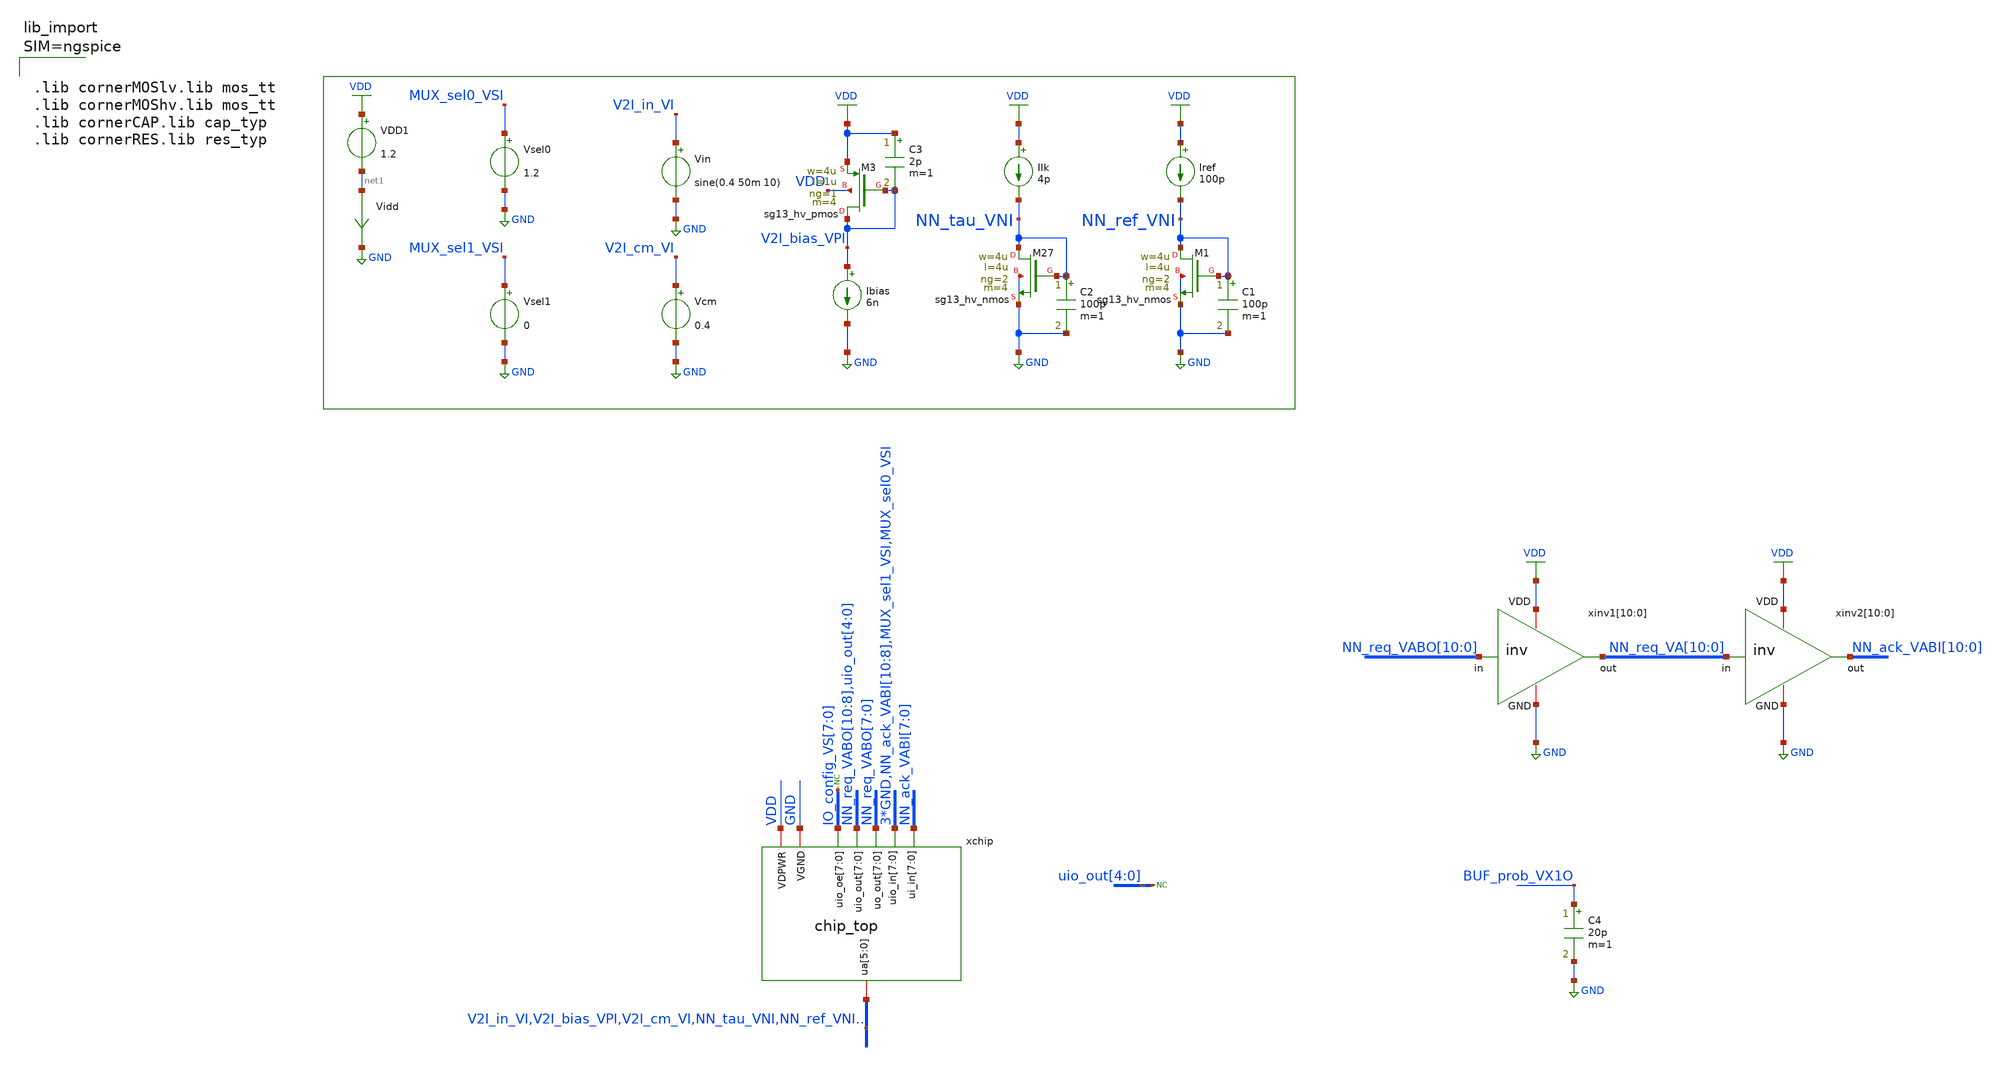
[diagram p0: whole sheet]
** sch_path: xschem/ncs-dpi-adexp/xschem/chip_top_tb.sch
**.subckt chip_top_tb
Ilk VDD NN_tau_VNI 4p
VDD1 VDD net1 1.2
Iref VDD NN_ref_VNI 100p
Vidd net1 GND 0
.save i(vidd)
XM27 NN_tau_VNI NN_tau_VNI GND GND sg13_hv_nmos w=4u l=4u ng=2 m=4 mm_ok=1
C2 NN_tau_VNI GND 100p m=1
XM1 NN_ref_VNI NN_ref_VNI GND GND sg13_hv_nmos w=4u l=4u ng=2 m=4 mm_ok=1
C1 NN_ref_VNI GND 100p m=1
XM3 V2I_bias_VPI V2I_bias_VPI VDD VDD sg13_hv_pmos w=4u l=1u ng=1 m=4 mm_ok=1
C3 VDD V2I_bias_VPI 2p m=1
Ibias V2I_bias_VPI GND 6n
Vcm V2I_cm_VI GND 0.4
Vin V2I_in_VI GND sine(0.4 50m 10)
C4 BUF_prob_VX1O GND 20p m=1
xinv1[10] VDD NN_req_VA[10] NN_req_VABO[10] GND inv
xinv1[9] VDD NN_req_VA[9] NN_req_VABO[9] GND inv
xinv1[8] VDD NN_req_VA[8] NN_req_VABO[8] GND inv
xinv1[7] VDD NN_req_VA[7] NN_req_VABO[7] GND inv
xinv1[6] VDD NN_req_VA[6] NN_req_VABO[6] GND inv
xinv1[5] VDD NN_req_VA[5] NN_req_VABO[5] GND inv
xinv1[4] VDD NN_req_VA[4] NN_req_VABO[4] GND inv
xinv1[3] VDD NN_req_VA[3] NN_req_VABO[3] GND inv
xinv1[2] VDD NN_req_VA[2] NN_req_VABO[2] GND inv
xinv1[1] VDD NN_req_VA[1] NN_req_VABO[1] GND inv
xinv1[0] VDD NN_req_VA[0] NN_req_VABO[0] GND inv
xinv2[10] VDD NN_ack_VABI[10] NN_req_VA[10] GND inv
xinv2[9] VDD NN_ack_VABI[9] NN_req_VA[9] GND inv
xinv2[8] VDD NN_ack_VABI[8] NN_req_VA[8] GND inv
xinv2[7] VDD NN_ack_VABI[7] NN_req_VA[7] GND inv
xinv2[6] VDD NN_ack_VABI[6] NN_req_VA[6] GND inv
xinv2[5] VDD NN_ack_VABI[5] NN_req_VA[5] GND inv
xinv2[4] VDD NN_ack_VABI[4] NN_req_VA[4] GND inv
xinv2[3] VDD NN_ack_VABI[3] NN_req_VA[3] GND inv
xinv2[2] VDD NN_ack_VABI[2] NN_req_VA[2] GND inv
xinv2[1] VDD NN_ack_VABI[1] NN_req_VA[1] GND inv
xinv2[0] VDD NN_ack_VABI[0] NN_req_VA[0] GND inv
xchip NN_ack_VABI[7] NN_ack_VABI[6] NN_ack_VABI[5] NN_ack_VABI[4] NN_ack_VABI[3] NN_ack_VABI[2]
+ NN_ack_VABI[1] NN_ack_VABI[0] V2I_in_VI V2I_bias_VPI V2I_cm_VI NN_tau_VNI NN_ref_VNI BUF_prob_VX1O VDD
+ NN_req_VABO[7] NN_req_VABO[6] NN_req_VABO[5] NN_req_VABO[4] NN_req_VABO[3] NN_req_VABO[2] NN_req_VABO[1]
+ NN_req_VABO[0] GND GND GND GND NN_ack_VABI[10] NN_ack_VABI[9] NN_ack_VABI[8] MUX_sel1_VSI MUX_sel0_VSI
+ NN_req_VABO[10] NN_req_VABO[9] NN_req_VABO[8] uio_out[4] uio_out[3] uio_out[2] uio_out[1] uio_out[0]
+ IO_config_VS[7] IO_config_VS[6] IO_config_VS[5] IO_config_VS[4] IO_config_VS[3] IO_config_VS[2] IO_config_VS[1]
+ IO_config_VS[0] chip_top
* noconn IO_config_VS[7:0]
* noconn uio_out[4:0]
Vsel1 MUX_sel1_VSI GND 0
Vsel0 MUX_sel0_VSI GND 1.2
**** begin user architecture code



.param temp=27

.ic V(NN_req_VABO[10])=1.2 V(NN_req_VABO[9])=1.2 V(NN_req_VABO[8])=1.2 V(NN_req_VABO[7])=1.2
+ V(NN_req_VABO[6])=1.2 V(NN_req_VABO[5])=1.2 V(NN_req_VABO[4])=1.2 V(NN_req_VABO[3])=1.2 V(NN_req_VABO[2])=1.2
+ V(NN_req_VABO[1])=1.2 V(NN_req_VABO[0])=1.2
.ic V(NN_ack_VABI[10])=1.2 V(NN_ack_VABI[9])=1.2 V(NN_ack_VABI[8])=1.2 V(NN_ack_VABI[7])=1.2
+ V(NN_ack_VABI[6])=1.2 V(NN_ack_VABI[5])=1.2 V(NN_ack_VABI[4])=1.2 V(NN_ack_VABI[3])=1.2 V(NN_ack_VABI[2])=1.2
+ V(NN_ack_VABI[1])=1.2 V(NN_ack_VABI[0])=1.2
.ic V(xchip.NN_mem_VNT[10])=0 V(xchip.NN_mem_VNT[9])=0 V(xchip.NN_mem_VNT[8])=0
+ V(xchip.NN_mem_VNT[7])=0 V(xchip.NN_mem_VNT[6])=0 V(xchip.NN_mem_VNT[5])=0 V(xchip.NN_mem_VNT[4])=0 V(xchip.NN_mem_VNT[3])=0
+ V(xchip.NN_mem_VNT[2])=0 V(xchip.NN_mem_VNT[1])=0 V(xchip.NN_mem_VNT[0])=0
.ic V(xchip.NN_refcap_VT[10])=0 V(xchip.NN_refcap_VT[9])=0 V(xchip.NN_refcap_VT[8])=0
+ V(xchip.NN_refcap_VT[7])=0 V(xchip.NN_refcap_VT[6])=0 V(xchip.NN_refcap_VT[5])=0 V(xchip.NN_refcap_VT[4])=0
+ V(xchip.NN_refcap_VT[3])=0 V(xchip.NN_refcap_VT[2])=0 V(xchip.NN_refcap_VT[1])=0 V(xchip.NN_refcap_VT[0])=0

.options gmin=1e-13
.options method=gear
.control

save V(NN_req_VABO[10]) V(NN_req_VABO[9]) V(NN_req_VABO[8]) V(NN_req_VABO[7]) V(NN_req_VABO[6])
+ V(NN_req_VABO[5]) V(NN_req_VABO[4]) V(NN_req_VABO[3]) V(NN_req_VABO[2]) V(NN_req_VABO[1]) V(NN_req_VABO[0])
save V(NN_ack_VABI[10]) V(NN_ack_VABI[9]) V(NN_ack_VABI[8]) V(NN_ack_VABI[7]) V(NN_ack_VABI[6])
+ V(NN_ack_VABI[5]) V(NN_ack_VABI[4]) V(NN_ack_VABI[3]) V(NN_ack_VABI[2]) V(NN_ack_VABI[1]) V(NN_ack_VABI[0])
save V(BUF_prob_VX1O) V(xchip.buf2mux_VTX1[1]) V(xchip.buf2mux_VTX1[0])
save V(xchip.NN_mem_VNT[10]) V(xchip.NN_mem_VNT[9]) V(xchip.NN_mem_VNT[8]) V(xchip.NN_mem_VNT[7])
+ V(xchip.NN_mem_VNT[6]) V(xchip.NN_mem_VNT[5]) V(xchip.NN_mem_VNT[4]) V(xchip.NN_mem_VNT[3]) V(xchip.NN_mem_VNT[2])
+ V(xchip.NN_mem_VNT[1]) V(xchip.NN_mem_VNT[0])
save V(xchip.NN_refcap_VT[10]) V(xchip.NN_refcap_VT[9]) V(xchip.NN_refcap_VT[8])
+ V(xchip.NN_refcap_VT[7]) V(xchip.NN_refcap_VT[6]) V(xchip.NN_refcap_VT[5]) V(xchip.NN_refcap_VT[4]) V(xchip.NN_refcap_VT[3])
+ V(xchip.NN_refcap_VT[2]) V(xchip.NN_refcap_VT[1]) V(xchip.NN_refcap_VT[0])
save V(IO_config_VS[7]) V(IO_config_VS[6]) V(IO_config_VS[5]) V(IO_config_VS[4]) V(IO_config_VS[3])
+ V(IO_config_VS[2]) V(IO_config_VS[1]) V(IO_config_VS[0])


tran 50n 100m
write chip_top_tb.raw
.endc







.lib cornerMOSlv.lib mos_tt
.lib cornerMOShv.lib mos_tt
.lib cornerCAP.lib cap_typ
.lib cornerRES.lib res_typ


**** end user architecture code
**.ends
.GLOBAL GND
.GLOBAL VDD
.end
